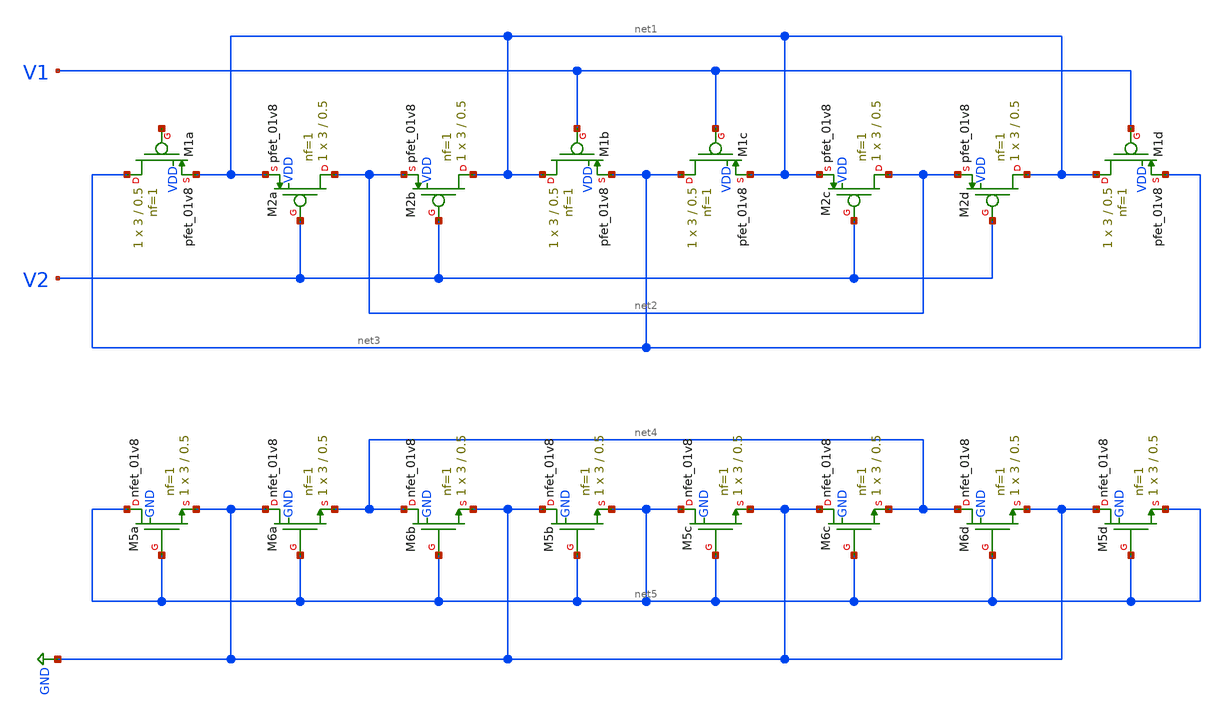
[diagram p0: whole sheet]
** sch_path: projects/current_mirror_diff_amp/xschem_ngspice/cmdiffamp.sch
**.subckt cmdiffamp
XM1a net3 net6 net1 VDD sky130_fd_pr__pfet_01v8 L=0.5 W=3 nf=1 ad='int((nf+1)/2) * W/nf * 0.29' as='int((nf+2)/2) * W/nf * 0.29'
+ pd='2*int((nf+1)/2) * (W/nf + 0.29)' ps='2*int((nf+2)/2) * (W/nf + 0.29)' nrd='0.29 / W' nrs='0.29 / W'
+ sa=0 sb=0 sd=0 mult=1 m=1
XM2a net2 V2 net1 VDD sky130_fd_pr__pfet_01v8 L=0.5 W=3 nf=1 ad='int((nf+1)/2) * W/nf * 0.29' as='int((nf+2)/2) * W/nf * 0.29'
+ pd='2*int((nf+1)/2) * (W/nf + 0.29)' ps='2*int((nf+2)/2) * (W/nf + 0.29)' nrd='0.29 / W' nrs='0.29 / W'
+ sa=0 sb=0 sd=0 mult=1 m=1
XM2b net1 V2 net2 VDD sky130_fd_pr__pfet_01v8 L=0.5 W=3 nf=1 ad='int((nf+1)/2) * W/nf * 0.29' as='int((nf+2)/2) * W/nf * 0.29'
+ pd='2*int((nf+1)/2) * (W/nf + 0.29)' ps='2*int((nf+2)/2) * (W/nf + 0.29)' nrd='0.29 / W' nrs='0.29 / W'
+ sa=0 sb=0 sd=0 mult=1 m=1
XM1b net1 V1 net3 VDD sky130_fd_pr__pfet_01v8 L=0.5 W=3 nf=1 ad='int((nf+1)/2) * W/nf * 0.29' as='int((nf+2)/2) * W/nf * 0.29'
+ pd='2*int((nf+1)/2) * (W/nf + 0.29)' ps='2*int((nf+2)/2) * (W/nf + 0.29)' nrd='0.29 / W' nrs='0.29 / W'
+ sa=0 sb=0 sd=0 mult=1 m=1
XM1c net3 V1 net1 VDD sky130_fd_pr__pfet_01v8 L=0.5 W=3 nf=1 ad='int((nf+1)/2) * W/nf * 0.29' as='int((nf+2)/2) * W/nf * 0.29'
+ pd='2*int((nf+1)/2) * (W/nf + 0.29)' ps='2*int((nf+2)/2) * (W/nf + 0.29)' nrd='0.29 / W' nrs='0.29 / W'
+ sa=0 sb=0 sd=0 mult=1 m=1
XM2c net2 V2 net1 VDD sky130_fd_pr__pfet_01v8 L=0.5 W=3 nf=1 ad='int((nf+1)/2) * W/nf * 0.29' as='int((nf+2)/2) * W/nf * 0.29'
+ pd='2*int((nf+1)/2) * (W/nf + 0.29)' ps='2*int((nf+2)/2) * (W/nf + 0.29)' nrd='0.29 / W' nrs='0.29 / W'
+ sa=0 sb=0 sd=0 mult=1 m=1
XM2d net1 V2 net2 VDD sky130_fd_pr__pfet_01v8 L=0.5 W=3 nf=1 ad='int((nf+1)/2) * W/nf * 0.29' as='int((nf+2)/2) * W/nf * 0.29'
+ pd='2*int((nf+1)/2) * (W/nf + 0.29)' ps='2*int((nf+2)/2) * (W/nf + 0.29)' nrd='0.29 / W' nrs='0.29 / W'
+ sa=0 sb=0 sd=0 mult=1 m=1
XM1d net1 V1 net3 VDD sky130_fd_pr__pfet_01v8 L=0.5 W=3 nf=1 ad='int((nf+1)/2) * W/nf * 0.29' as='int((nf+2)/2) * W/nf * 0.29'
+ pd='2*int((nf+1)/2) * (W/nf + 0.29)' ps='2*int((nf+2)/2) * (W/nf + 0.29)' nrd='0.29 / W' nrs='0.29 / W'
+ sa=0 sb=0 sd=0 mult=1 m=1
XM5a net5 net5 GND GND sky130_fd_pr__nfet_01v8 L=0.5 W=3 nf=1 ad='int((nf+1)/2) * W/nf * 0.29' as='int((nf+2)/2) * W/nf * 0.29'
+ pd='2*int((nf+1)/2) * (W/nf + 0.29)' ps='2*int((nf+2)/2) * (W/nf + 0.29)' nrd='0.29 / W' nrs='0.29 / W'
+ sa=0 sb=0 sd=0 mult=1 m=1
XM6a GND net5 net4 GND sky130_fd_pr__nfet_01v8 L=0.5 W=3 nf=1 ad='int((nf+1)/2) * W/nf * 0.29' as='int((nf+2)/2) * W/nf * 0.29'
+ pd='2*int((nf+1)/2) * (W/nf + 0.29)' ps='2*int((nf+2)/2) * (W/nf + 0.29)' nrd='0.29 / W' nrs='0.29 / W'
+ sa=0 sb=0 sd=0 mult=1 m=1
XM6b net4 net5 GND GND sky130_fd_pr__nfet_01v8 L=0.5 W=3 nf=1 ad='int((nf+1)/2) * W/nf * 0.29' as='int((nf+2)/2) * W/nf * 0.29'
+ pd='2*int((nf+1)/2) * (W/nf + 0.29)' ps='2*int((nf+2)/2) * (W/nf + 0.29)' nrd='0.29 / W' nrs='0.29 / W'
+ sa=0 sb=0 sd=0 mult=1 m=1
XM5b GND net5 net5 GND sky130_fd_pr__nfet_01v8 L=0.5 W=3 nf=1 ad='int((nf+1)/2) * W/nf * 0.29' as='int((nf+2)/2) * W/nf * 0.29'
+ pd='2*int((nf+1)/2) * (W/nf + 0.29)' ps='2*int((nf+2)/2) * (W/nf + 0.29)' nrd='0.29 / W' nrs='0.29 / W'
+ sa=0 sb=0 sd=0 mult=1 m=1
XM5c net5 net5 GND GND sky130_fd_pr__nfet_01v8 L=0.5 W=3 nf=1 ad='int((nf+1)/2) * W/nf * 0.29' as='int((nf+2)/2) * W/nf * 0.29'
+ pd='2*int((nf+1)/2) * (W/nf + 0.29)' ps='2*int((nf+2)/2) * (W/nf + 0.29)' nrd='0.29 / W' nrs='0.29 / W'
+ sa=0 sb=0 sd=0 mult=1 m=1
XM6c GND net5 net4 GND sky130_fd_pr__nfet_01v8 L=0.5 W=3 nf=1 ad='int((nf+1)/2) * W/nf * 0.29' as='int((nf+2)/2) * W/nf * 0.29'
+ pd='2*int((nf+1)/2) * (W/nf + 0.29)' ps='2*int((nf+2)/2) * (W/nf + 0.29)' nrd='0.29 / W' nrs='0.29 / W'
+ sa=0 sb=0 sd=0 mult=1 m=1
XM6d net4 net5 GND GND sky130_fd_pr__nfet_01v8 L=0.5 W=3 nf=1 ad='int((nf+1)/2) * W/nf * 0.29' as='int((nf+2)/2) * W/nf * 0.29'
+ pd='2*int((nf+1)/2) * (W/nf + 0.29)' ps='2*int((nf+2)/2) * (W/nf + 0.29)' nrd='0.29 / W' nrs='0.29 / W'
+ sa=0 sb=0 sd=0 mult=1 m=1
XM5d GND net5 net5 GND sky130_fd_pr__nfet_01v8 L=0.5 W=3 nf=1 ad='int((nf+1)/2) * W/nf * 0.29' as='int((nf+2)/2) * W/nf * 0.29'
+ pd='2*int((nf+1)/2) * (W/nf + 0.29)' ps='2*int((nf+2)/2) * (W/nf + 0.29)' nrd='0.29 / W' nrs='0.29 / W'
+ sa=0 sb=0 sd=0 mult=1 m=1
**.ends
.GLOBAL GND
.end
